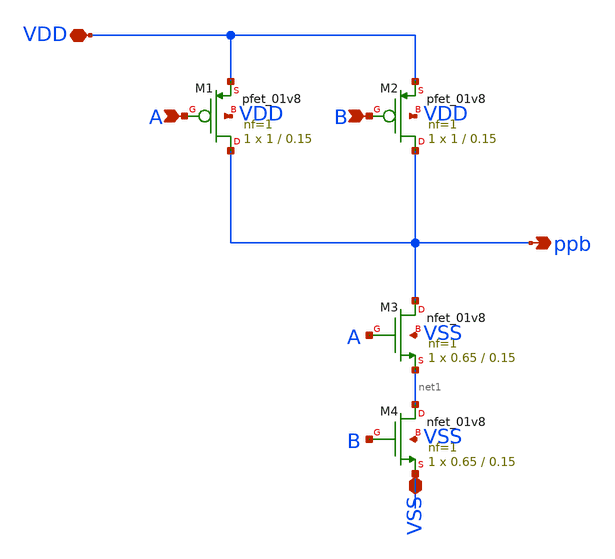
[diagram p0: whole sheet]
** sch_path: xschem/nand2.sch
**.subckt nand2 A B VDD VSS ppb
*.ipin A
*.ipin B
*.iopin VDD
*.iopin VSS
*.opin ppb
XM1 ppb A VDD VDD sky130_fd_pr__pfet_01v8 L=0.15 W=1 nf=1 ad='int((1 + 1)/2) * 1 / 1 * 0.29' as='int((1 + 2)/2) * 1 / 1 * 0.29'
+ pd='2*int((1 + 1)/2) * (1 / 1 + 0.29)' ps='2*int((1 + 2)/2) * (1 / 1 + 0.29)' nrd='0.29 / 1 ' nrs='0.29 / 1 '
+ sa=0 sb=0 sd=0 mult=1 m=1
XM2 ppb B VDD VDD sky130_fd_pr__pfet_01v8 L=0.15 W=1 nf=1 ad='int((1 + 1)/2) * 1 / 1 * 0.29' as='int((1 + 2)/2) * 1 / 1 * 0.29'
+ pd='2*int((1 + 1)/2) * (1 / 1 + 0.29)' ps='2*int((1 + 2)/2) * (1 / 1 + 0.29)' nrd='0.29 / 1 ' nrs='0.29 / 1 '
+ sa=0 sb=0 sd=0 mult=1 m=1
XM3 ppb A net1 VSS sky130_fd_pr__nfet_01v8 L=0.15 W=0.65 nf=1 ad='int((1 + 1)/2) * 0.65 / 1 * 0.29' as='int((1 + 2)/2) * 0.65 / 1 * 0.29'
+ pd='2*int((1 + 1)/2) * (0.65 / 1 + 0.29)' ps='2*int((1 + 2)/2) * (0.65 / 1 + 0.29)' nrd='0.29 / 0.65 '
+ nrs='0.29 / 0.65 ' sa=0 sb=0 sd=0 mult=1 m=1
XM4 net1 B VSS VSS sky130_fd_pr__nfet_01v8 L=0.15 W=0.65 nf=1 ad='int((1 + 1)/2) * 0.65 / 1 * 0.29' as='int((1 + 2)/2) * 0.65 / 1 * 0.29'
+ pd='2*int((1 + 1)/2) * (0.65 / 1 + 0.29)' ps='2*int((1 + 2)/2) * (0.65 / 1 + 0.29)' nrd='0.29 / 0.65 '
+ nrs='0.29 / 0.65 ' sa=0 sb=0 sd=0 mult=1 m=1
**.ends
.end
